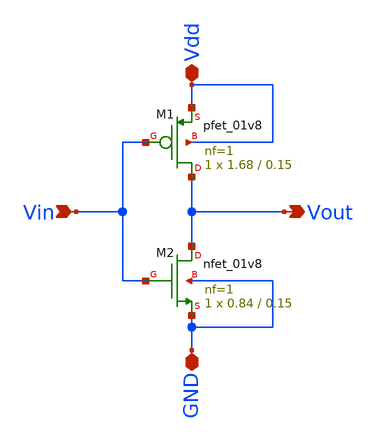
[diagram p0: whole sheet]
** sch_path: xschem_project/inv_x2/inv_x2.sch
**.subckt inv_x2 Vin Vout Vdd GND
*.ipin Vin
*.opin Vout
*.iopin Vdd
*.iopin GND
XM1 Vout Vin Vdd Vdd sky130_fd_pr__pfet_01v8 L=0.15 W=1.68 nf=1 ad='int((1 + 1)/2) * 1.68 / 1 * 0.29'
+ as='int((1 + 2)/2) * 1.68 / 1 * 0.29' pd='2*int((1 + 1)/2) * (1.68 / 1 + 0.29)' ps='2*int((1 + 2)/2) * (1.68 / 1 + 0.29)'
+ nrd='0.29 / 1.68 ' nrs='0.29 / 1.68 ' sa=0 sb=0 sd=0 mult=1 m=1
XM2 Vout Vin GND GND sky130_fd_pr__nfet_01v8 L=0.15 W=0.84 nf=1 ad='int((1 + 1)/2) * 0.84 / 1 * 0.29'
+ as='int((1 + 2)/2) * 0.84 / 1 * 0.29' pd='2*int((1 + 1)/2) * (0.84 / 1 + 0.29)' ps='2*int((1 + 2)/2) * (0.84 / 1 + 0.29)'
+ nrd='0.29 / 0.84 ' nrs='0.29 / 0.84 ' sa=0 sb=0 sd=0 mult=1 m=1
**.ends
.end
